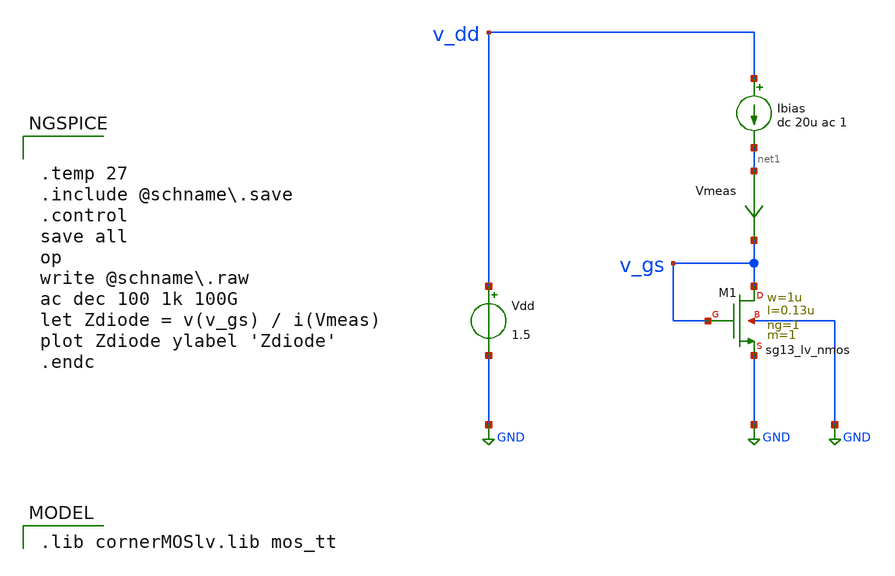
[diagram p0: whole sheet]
** sch_path: xschem/mosfet_diode_impedance.sch
* (c) 2024-2025 Harald Pretl, Apache-2.0 license
**.subckt mosfet_diode_impedance
Vdd v_dd GND 1.5
XM1 v_gs v_gs GND GND sg13_lv_nmos w=1u l=0.13u ng=1 m=1 mm_ok=1
Ibias v_dd net1 dc 20u ac 1
Vmeas net1 v_gs 0
.save i(vmeas)
**** begin user architecture code
 .lib cornerMOSlv.lib mos_tt



.temp 27
.include @schname\.save
.control
save all
op
write @schname\.raw
ac dec 100 1k 100G
let Zdiode = v(v_gs) / i(Vmeas)
plot Zdiode ylabel 'Zdiode'
.endc


**** end user architecture code
**.ends
.GLOBAL GND
.end
